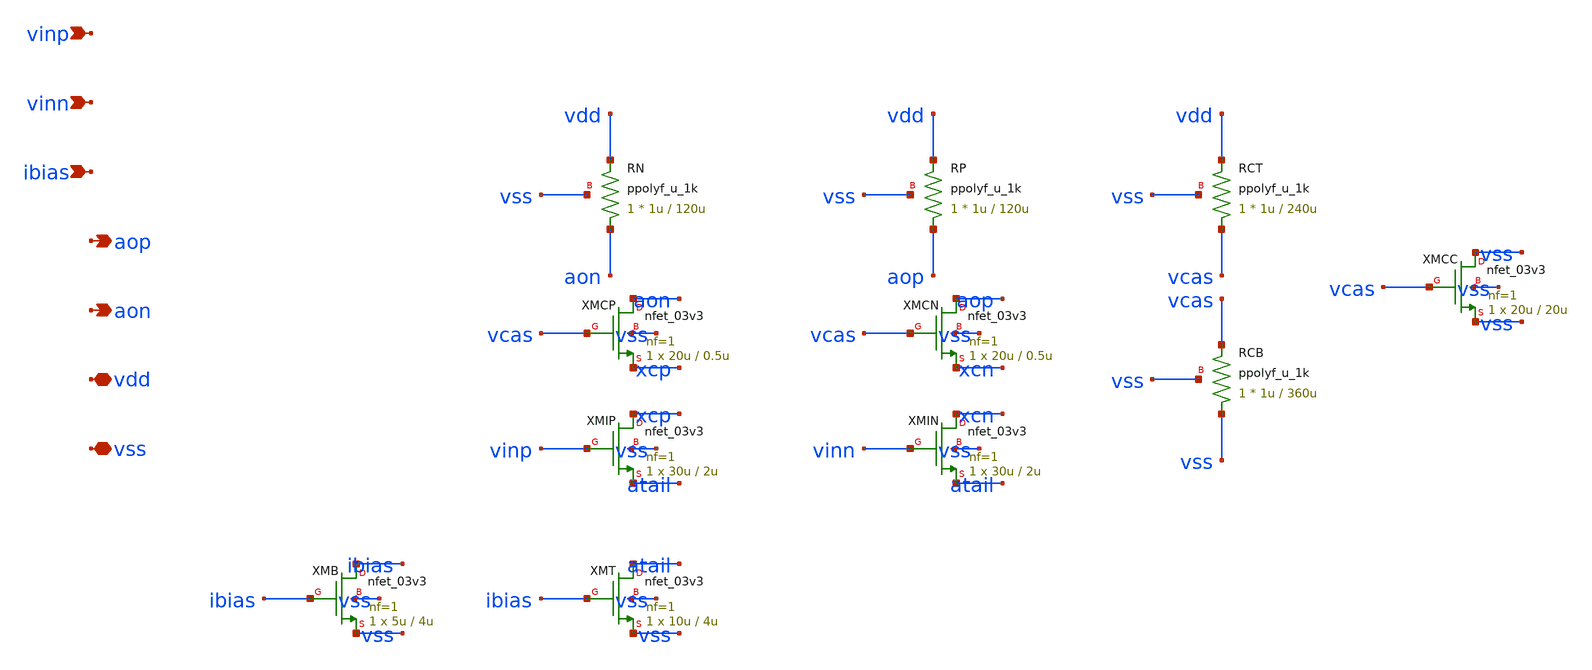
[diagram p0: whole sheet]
** sch_path: design/proposed/dr0004-cascode/comparator_dut_analog.sch
**.subckt comparator_dut_analog vinp vinn ibias aop aon vdd vss
*.ipin vinp
*.ipin vinn
*.ipin ibias
*.opin aop
*.opin aon
*.iopin vdd
*.iopin vss
XMB ibias ibias vss vss nfet_03v3 L=4u W=5u nf=1 ad='int((nf+1)/2) * W/nf * 0.18u' as='int((nf+2)/2) * W/nf * 0.18u'
+ pd='2*int((nf+1)/2) * (W/nf + 0.18u)' ps='2*int((nf+2)/2) * (W/nf + 0.18u)' nrd='0.18u / W' nrs='0.18u / W'
+ sa=0 sb=0 sd=0 m=1
XMT atail ibias vss vss nfet_03v3 L=4u W=10u nf=1 ad='int((nf+1)/2) * W/nf * 0.18u' as='int((nf+2)/2) * W/nf * 0.18u'
+ pd='2*int((nf+1)/2) * (W/nf + 0.18u)' ps='2*int((nf+2)/2) * (W/nf + 0.18u)' nrd='0.18u / W' nrs='0.18u / W'
+ sa=0 sb=0 sd=0 m=1
XMIP xcp vinp atail vss nfet_03v3 L=2u W=30u nf=1 ad='int((nf+1)/2) * W/nf * 0.18u' as='int((nf+2)/2) * W/nf * 0.18u'
+ pd='2*int((nf+1)/2) * (W/nf + 0.18u)' ps='2*int((nf+2)/2) * (W/nf + 0.18u)' nrd='0.18u / W' nrs='0.18u / W'
+ sa=0 sb=0 sd=0 m=1
XMIN xcn vinn atail vss nfet_03v3 L=2u W=30u nf=1 ad='int((nf+1)/2) * W/nf * 0.18u' as='int((nf+2)/2) * W/nf * 0.18u'
+ pd='2*int((nf+1)/2) * (W/nf + 0.18u)' ps='2*int((nf+2)/2) * (W/nf + 0.18u)' nrd='0.18u / W' nrs='0.18u / W'
+ sa=0 sb=0 sd=0 m=1
XRN aon vdd vss ppolyf_u_1k r_width=1u r_length=120u m=1
XRP aop vdd vss ppolyf_u_1k r_width=1u r_length=120u m=1
XMCP aon vcas xcp vss nfet_03v3 L=0.5u W=20u nf=1 ad='int((nf+1)/2) * W/nf * 0.18u' as='int((nf+2)/2) * W/nf * 0.18u'
+ pd='2*int((nf+1)/2) * (W/nf + 0.18u)' ps='2*int((nf+2)/2) * (W/nf + 0.18u)' nrd='0.18u / W' nrs='0.18u / W'
+ sa=0 sb=0 sd=0 m=1
XMCN aop vcas xcn vss nfet_03v3 L=0.5u W=20u nf=1 ad='int((nf+1)/2) * W/nf * 0.18u' as='int((nf+2)/2) * W/nf * 0.18u'
+ pd='2*int((nf+1)/2) * (W/nf + 0.18u)' ps='2*int((nf+2)/2) * (W/nf + 0.18u)' nrd='0.18u / W' nrs='0.18u / W'
+ sa=0 sb=0 sd=0 m=1
XRCT vcas vdd vss ppolyf_u_1k r_width=1u r_length=240u m=1
XRCB vss vcas vss ppolyf_u_1k r_width=1u r_length=360u m=1
XMCC vss vcas vss vss nfet_03v3 L=20u W=20u nf=1 ad='int((nf+1)/2) * W/nf * 0.18u' as='int((nf+2)/2) * W/nf * 0.18u'
+ pd='2*int((nf+1)/2) * (W/nf + 0.18u)' ps='2*int((nf+2)/2) * (W/nf + 0.18u)' nrd='0.18u / W' nrs='0.18u / W'
+ sa=0 sb=0 sd=0 m=1
**.ends
.end
